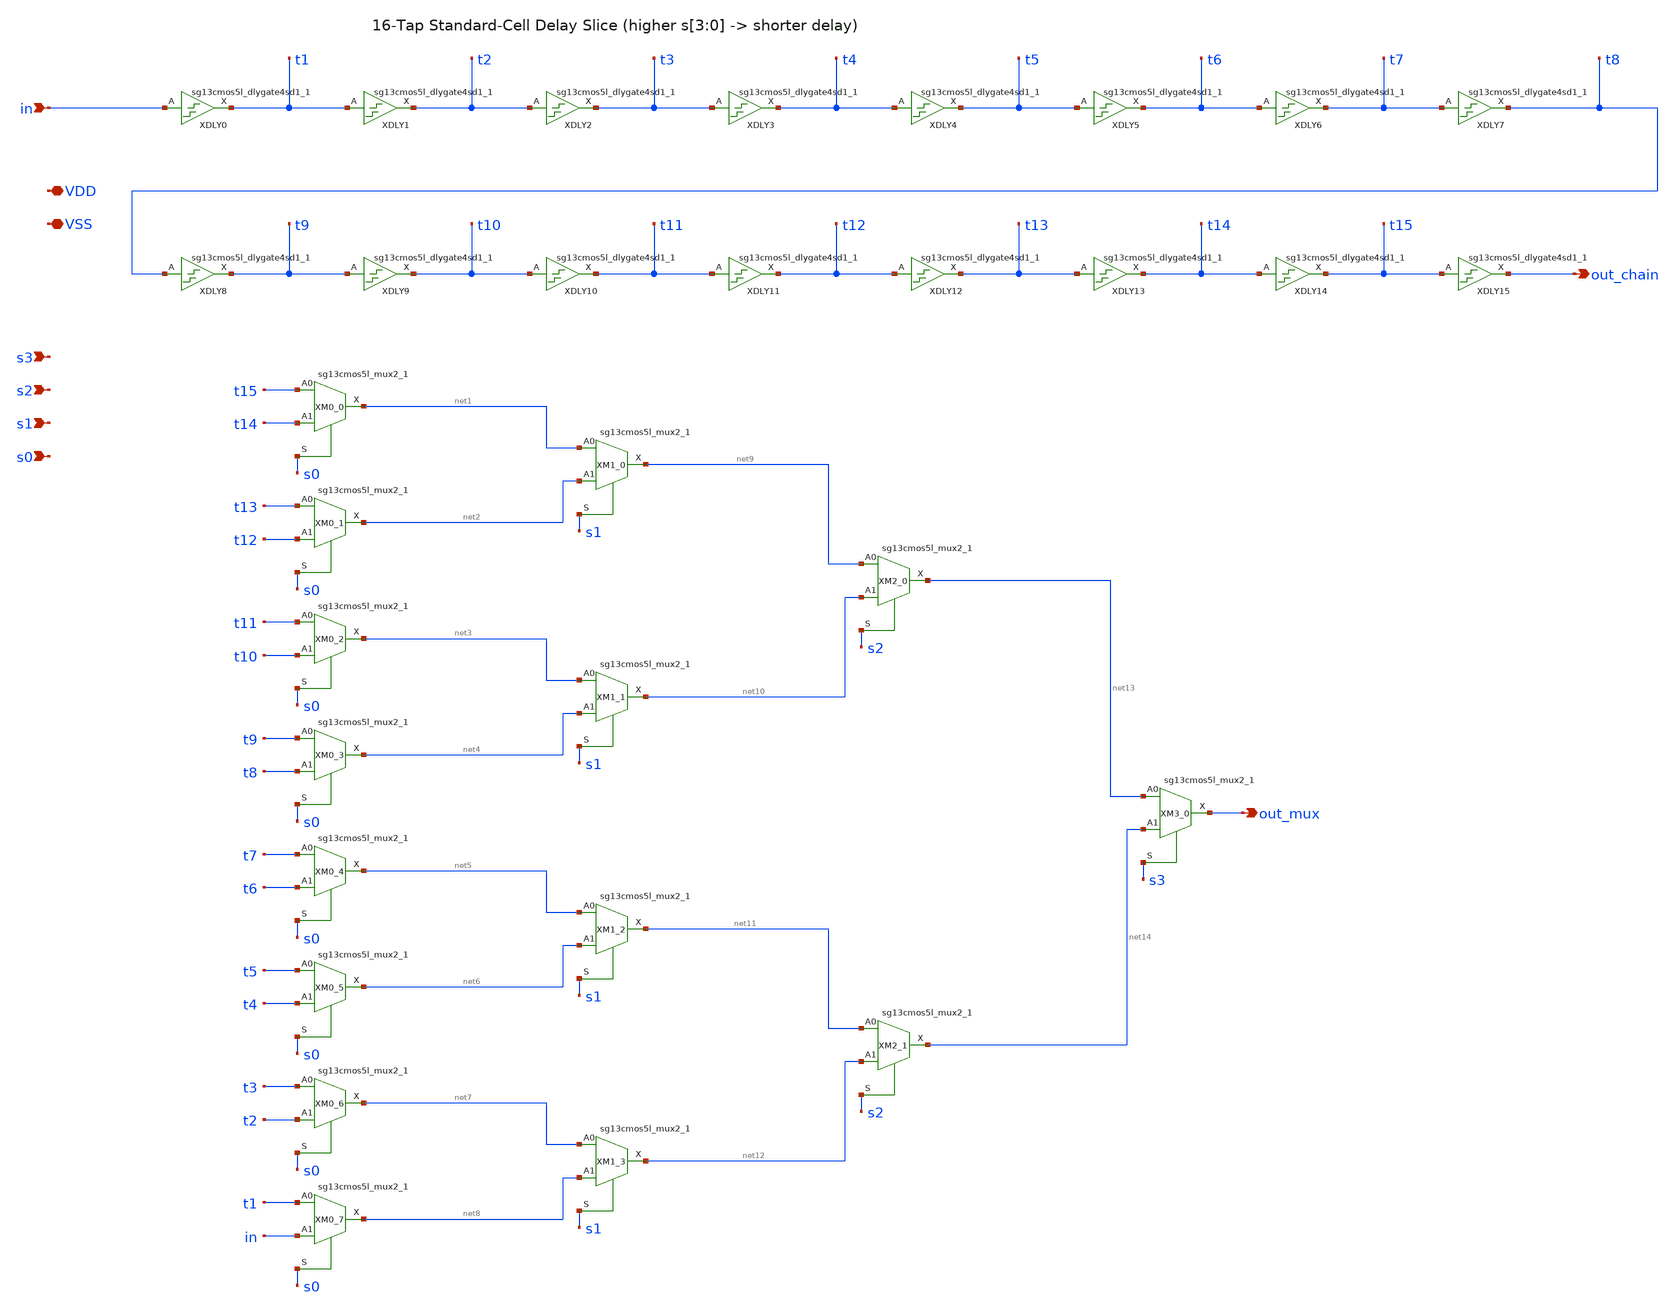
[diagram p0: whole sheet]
** sch_path: analog/osc_ring_std/tap_chain_16.sch
**.subckt tap_chain_16 VDD VSS in s3 s2 s1 s0 out_chain out_mux
*.iopin VDD
*.iopin VSS
*.ipin in
*.ipin s3
*.ipin s2
*.ipin s1
*.ipin s0
*.opin out_chain
*.opin out_mux
XDLY0 t1 in VDD VSS sg13cmos5l_dlygate4sd1_1
XDLY1 t2 t1 VDD VSS sg13cmos5l_dlygate4sd1_1
XDLY2 t3 t2 VDD VSS sg13cmos5l_dlygate4sd1_1
XDLY3 t4 t3 VDD VSS sg13cmos5l_dlygate4sd1_1
XDLY4 t5 t4 VDD VSS sg13cmos5l_dlygate4sd1_1
XDLY5 t6 t5 VDD VSS sg13cmos5l_dlygate4sd1_1
XDLY6 t7 t6 VDD VSS sg13cmos5l_dlygate4sd1_1
XDLY7 t8 t7 VDD VSS sg13cmos5l_dlygate4sd1_1
XDLY8 t9 t8 VDD VSS sg13cmos5l_dlygate4sd1_1
XDLY9 t10 t9 VDD VSS sg13cmos5l_dlygate4sd1_1
XDLY10 t11 t10 VDD VSS sg13cmos5l_dlygate4sd1_1
XDLY11 t12 t11 VDD VSS sg13cmos5l_dlygate4sd1_1
XDLY12 t13 t12 VDD VSS sg13cmos5l_dlygate4sd1_1
XDLY13 t14 t13 VDD VSS sg13cmos5l_dlygate4sd1_1
XDLY14 t15 t14 VDD VSS sg13cmos5l_dlygate4sd1_1
XDLY15 out_chain t15 VDD VSS sg13cmos5l_dlygate4sd1_1
XM0_0 net1 t15 t14 s0 VDD VSS sg13cmos5l_mux2_1
XM0_1 net2 t13 t12 s0 VDD VSS sg13cmos5l_mux2_1
XM0_2 net3 t11 t10 s0 VDD VSS sg13cmos5l_mux2_1
XM0_3 net4 t9 t8 s0 VDD VSS sg13cmos5l_mux2_1
XM0_4 net5 t7 t6 s0 VDD VSS sg13cmos5l_mux2_1
XM0_5 net6 t5 t4 s0 VDD VSS sg13cmos5l_mux2_1
XM0_6 net7 t3 t2 s0 VDD VSS sg13cmos5l_mux2_1
XM0_7 net8 t1 in s0 VDD VSS sg13cmos5l_mux2_1
XM1_0 net9 net1 net2 s1 VDD VSS sg13cmos5l_mux2_1
XM1_1 net10 net3 net4 s1 VDD VSS sg13cmos5l_mux2_1
XM1_2 net11 net5 net6 s1 VDD VSS sg13cmos5l_mux2_1
XM1_3 net12 net7 net8 s1 VDD VSS sg13cmos5l_mux2_1
XM2_0 net13 net9 net10 s2 VDD VSS sg13cmos5l_mux2_1
XM2_1 net14 net11 net12 s2 VDD VSS sg13cmos5l_mux2_1
XM3_0 out_mux net13 net14 s3 VDD VSS sg13cmos5l_mux2_1
**.ends
.end
